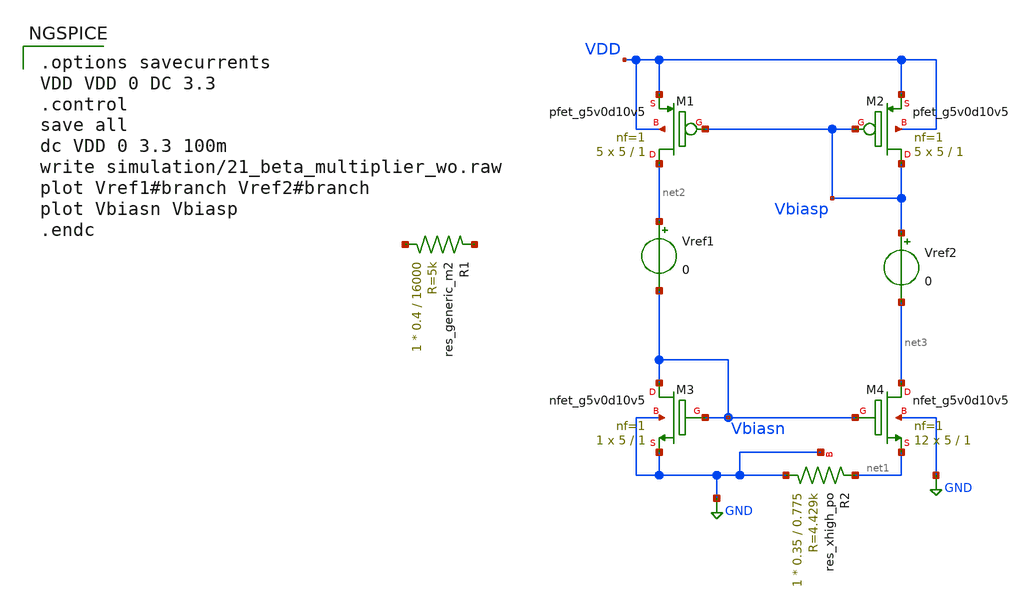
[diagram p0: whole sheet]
** sch_path: xschem/21_beta_multiplier_wo.sch
**.subckt 21_beta_multiplier_wo
R1 net4 net5 sky130_fd_pr__res_generic_m2 W=0.4 L=16000 m=1
XM1 net2 Vbiasp VDD VDD sky130_fd_pr__pfet_g5v0d10v5 L=1 W=5 nf=1 ad='int((nf+1)/2) * W/nf * 0.29' as='int((nf+2)/2) * W/nf * 0.29'
+ pd='2*int((nf+1)/2) * (W/nf + 0.29)' ps='2*int((nf+2)/2) * (W/nf + 0.29)' nrd='0.29 / W' nrs='0.29 / W'
+ sa=0 sb=0 sd=0 mult=5 m=5
XM3 Vbiasn Vbiasn GND GND sky130_fd_pr__nfet_g5v0d10v5 L=1 W=5 nf=1 ad='int((nf+1)/2) * W/nf * 0.29'
+ as='int((nf+2)/2) * W/nf * 0.29' pd='2*int((nf+1)/2) * (W/nf + 0.29)' ps='2*int((nf+2)/2) * (W/nf + 0.29)'
+ nrd='0.29 / W' nrs='0.29 / W' sa=0 sb=0 sd=0 mult=1 m=1
XM2 Vbiasp Vbiasp VDD VDD sky130_fd_pr__pfet_g5v0d10v5 L=1 W=5 nf=1 ad='int((nf+1)/2) * W/nf * 0.29'
+ as='int((nf+2)/2) * W/nf * 0.29' pd='2*int((nf+1)/2) * (W/nf + 0.29)' ps='2*int((nf+2)/2) * (W/nf + 0.29)'
+ nrd='0.29 / W' nrs='0.29 / W' sa=0 sb=0 sd=0 mult=5 m=5
XM4 net3 Vbiasn net1 GND sky130_fd_pr__nfet_g5v0d10v5 L=1 W=5 nf=1 ad='int((nf+1)/2) * W/nf * 0.29' as='int((nf+2)/2) * W/nf * 0.29'
+ pd='2*int((nf+1)/2) * (W/nf + 0.29)' ps='2*int((nf+2)/2) * (W/nf + 0.29)' nrd='0.29 / W' nrs='0.29 / W'
+ sa=0 sb=0 sd=0 mult=12 m=12
Vref1 net2 Vbiasn 0
Vref2 Vbiasp net3 0
XR2 GND net1 GND sky130_fd_pr__res_xhigh_po W=0.35 L=0.775 mult=1 m=1
**** begin user architecture code

.options savecurrents
VDD VDD 0 DC 3.3
.control
save all
dc VDD 0 3.3 100m
write simulation/21_beta_multiplier_wo.raw
plot Vref1#branch Vref2#branch
plot Vbiasn Vbiasp
.endc



** opencircuitdesign pdks install
.lib $::SKYWATER_MODELS/sky130.lib.spice tt


**** end user architecture code
**.ends
.GLOBAL GND
.end
